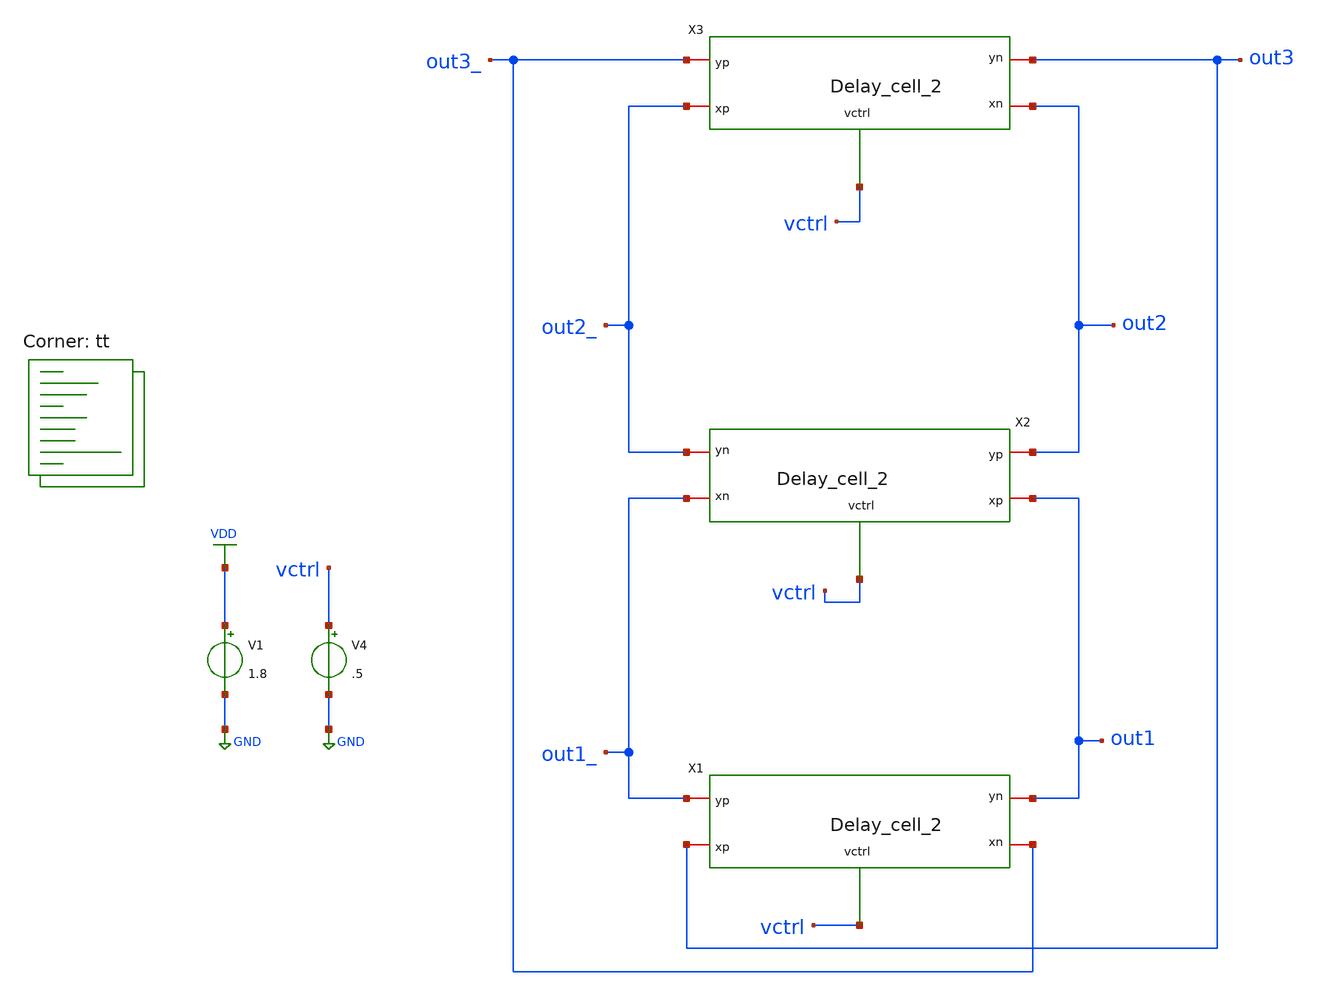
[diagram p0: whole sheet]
** sch_path: pll/ring_vco_lib/delay_cell/xschem/RO2.sch
**.subckt RO2
V1 VDD GND 1.8
X1 out1_ out1 out3 out3_ vctrl Delay_cell_2
X3 out3_ out3 out2_ out2 vctrl Delay_cell_2
X2 out2 out2_ out1 out1_ vctrl Delay_cell_2
V4 vctrl GND .5
**** begin user architecture code



.tran 1p 10n
.probe I(x1)
.plot V(out1)
.save all

.lib $::SKYWATER_MODELS/sky130.lib.spice tt
**** end user architecture code
**.ends

* expanding   symbol:  Delay_cell_2.sym # of pins=5
** sym_path: delay_cell/Delay_cell_2.sym
** sch_path: delay_cell/Delay_cell_2.sch
.subckt Delay_cell_2 yp yn xp xn vctrl
*.iopin yp
*.iopin xn
*.iopin xp
*.iopin yn
*.ipin vctrl
R2 yp net1 800 m=1
R1 yn net2 800 m=1
XM4 net3 net3 VDD VDD sky130_fd_pr__pfet_01v8 L=0.15 W=12 nf=1 ad='int((nf+1)/2) * W/nf * 0.29' as='int((nf+2)/2) * W/nf * 0.29'
+ pd='2*int((nf+1)/2) * (W/nf + 0.29)' ps='2*int((nf+2)/2) * (W/nf + 0.29)' nrd='0.29 / W' nrs='0.29 / W'
+ sa=0 sb=0 sd=0 mult=1 m=1
XM7 net3 vctrl GND GND sky130_fd_pr__nfet_01v8 L=0.15 W=.5 nf=1 ad='int((nf+1)/2) * W/nf * 0.29' as='int((nf+2)/2) * W/nf * 0.29'
+ pd='2*int((nf+1)/2) * (W/nf + 0.29)' ps='2*int((nf+2)/2) * (W/nf + 0.29)' nrd='0.29 / W' nrs='0.29 / W'
+ sa=0 sb=0 sd=0 mult=1 m=1
C1 yn GND .57e-15 m=1
C2 yp GND .57e-15 m=1
XM1 net1 xn GND GND sky130_fd_pr__nfet_01v8 L=0.15 W=1.5 nf=1 ad='int((nf+1)/2) * W/nf * 0.29' as='int((nf+2)/2) * W/nf * 0.29'
+ pd='2*int((nf+1)/2) * (W/nf + 0.29)' ps='2*int((nf+2)/2) * (W/nf + 0.29)' nrd='0.29 / W' nrs='0.29 / W'
+ sa=0 sb=0 sd=0 mult=1 m=1
XM6 net2 xp GND GND sky130_fd_pr__nfet_01v8 L=0.15 W=1.5 nf=1 ad='int((nf+1)/2) * W/nf * 0.29' as='int((nf+2)/2) * W/nf * 0.29'
+ pd='2*int((nf+1)/2) * (W/nf + 0.29)' ps='2*int((nf+2)/2) * (W/nf + 0.29)' nrd='0.29 / W' nrs='0.29 / W'
+ sa=0 sb=0 sd=0 mult=1 m=1
XM2 yp net3 VDD VDD sky130_fd_pr__pfet_01v8 L=0.15 W=.5 nf=1 ad='int((nf+1)/2) * W/nf * 0.29' as='int((nf+2)/2) * W/nf * 0.29'
+ pd='2*int((nf+1)/2) * (W/nf + 0.29)' ps='2*int((nf+2)/2) * (W/nf + 0.29)' nrd='0.29 / W' nrs='0.29 / W'
+ sa=0 sb=0 sd=0 mult=1 m=1
XM3 yn net1 VDD VDD sky130_fd_pr__pfet_01v8 L=0.15 W=1 nf=1 ad='int((nf+1)/2) * W/nf * 0.29' as='int((nf+2)/2) * W/nf * 0.29'
+ pd='2*int((nf+1)/2) * (W/nf + 0.29)' ps='2*int((nf+2)/2) * (W/nf + 0.29)' nrd='0.29 / W' nrs='0.29 / W'
+ sa=0 sb=0 sd=0 mult=1 m=1
XM5 yp net2 VDD VDD sky130_fd_pr__pfet_01v8 L=0.15 W=1 nf=1 ad='int((nf+1)/2) * W/nf * 0.29' as='int((nf+2)/2) * W/nf * 0.29'
+ pd='2*int((nf+1)/2) * (W/nf + 0.29)' ps='2*int((nf+2)/2) * (W/nf + 0.29)' nrd='0.29 / W' nrs='0.29 / W'
+ sa=0 sb=0 sd=0 mult=1 m=1
XM8 yn net3 VDD VDD sky130_fd_pr__pfet_01v8 L=0.15 W=.5 nf=1 ad='int((nf+1)/2) * W/nf * 0.29' as='int((nf+2)/2) * W/nf * 0.29'
+ pd='2*int((nf+1)/2) * (W/nf + 0.29)' ps='2*int((nf+2)/2) * (W/nf + 0.29)' nrd='0.29 / W' nrs='0.29 / W'
+ sa=0 sb=0 sd=0 mult=1 m=1
.ends

.GLOBAL VDD
.GLOBAL GND
.end
